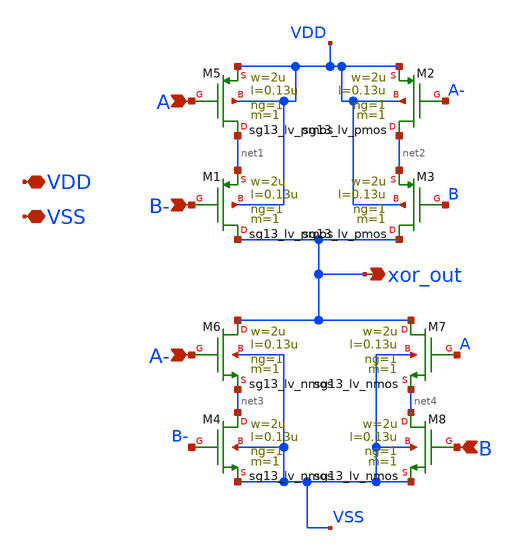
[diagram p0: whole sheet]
** sch_path: xschem/robs_xor.sch
**.subckt robs_xor xor_out A B- A- B VDD VSS
*.opin xor_out
*.ipin A
*.ipin B-
*.ipin A-
*.ipin B
*.iopin VDD
*.iopin VSS
XM5 net1 A VDD VDD sg13_lv_pmos w=2u l=0.13u ng=1 m=1 mm_ok=1
XM6 xor_out A- net3 VSS sg13_lv_nmos w=2u l=0.13u ng=1 m=1 mm_ok=1
XM1 xor_out B- net1 VDD sg13_lv_pmos w=2u l=0.13u ng=1 m=1 mm_ok=1
XM2 net2 A- VDD VDD sg13_lv_pmos w=2u l=0.13u ng=1 m=1 mm_ok=1
XM3 xor_out B net2 VDD sg13_lv_pmos w=2u l=0.13u ng=1 m=1 mm_ok=1
XM4 net3 B- VSS VSS sg13_lv_nmos w=2u l=0.13u ng=1 m=1 mm_ok=1
XM7 xor_out A net4 VSS sg13_lv_nmos w=2u l=0.13u ng=1 m=1 mm_ok=1
XM8 net4 B VSS VSS sg13_lv_nmos w=2u l=0.13u ng=1 m=1 mm_ok=1
**.ends
.end
